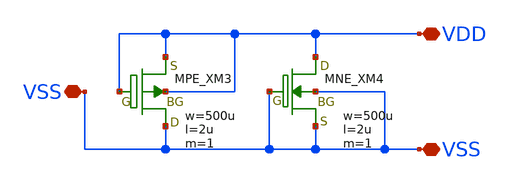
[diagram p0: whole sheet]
** sch_path: libs.tech/xschem/TR-1um_frame/OSS_ESD_5V_VSS.sch
**.subckt OSS_ESD_5V_VSS VSS VDD VSS
*.iopin VSS
*.iopin VDD
*.iopin VSS
XXM3 VSS VDD VDD VDD MPE w=500u l=2u as=0 ad=0 ps=0 pd=0 nrd=0 nrs=0 m=1
XXM4 VDD VSS VSS VSS MNE w=500u l=2u as=0 ad=0 ps=0 pd=0 nrd=0 nrs=0 m=1
**.ends
.end
